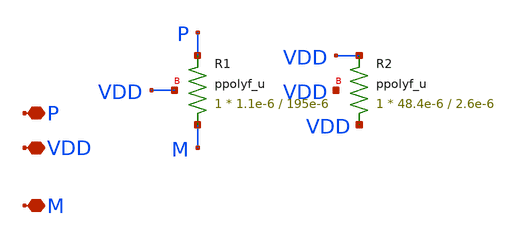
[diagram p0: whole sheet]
** sch_path: PLL-main/schematic/xschem/Res_74k.sch
**.subckt Res_74k P VDD M
*.iopin P
*.iopin VDD
*.iopin M
XR1 M P VDD ppolyf_u r_width=1.1e-6 r_length=195e-6 m=1
XR2 VDD VDD VDD ppolyf_u r_width=48.4e-6 r_length=2.6e-6 m=1
**.ends
.end
